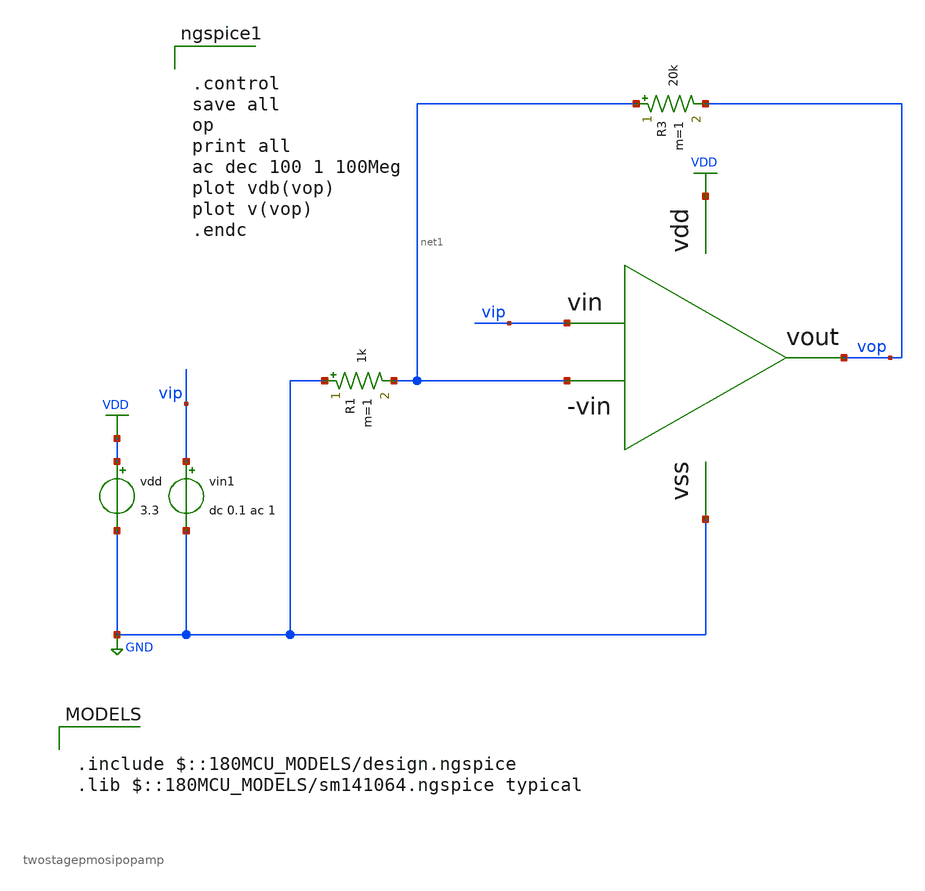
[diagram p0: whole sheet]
** sch_path: designs/libs/OTA/pmosota_VF_tb.sch
**.subckt pmosota_VF_tb
vdd VDD GND 3.3
xOTA1 vip VDD net1 vop GND twostagepmosipopamp
R3 net1 vop 20k m=1
R1 GND net1 1k m=1
vin1 vip GND dc 0.1 ac 1
**** begin user architecture code

.include $::180MCU_MODELS/design.ngspice
.lib $::180MCU_MODELS/sm141064.ngspice typical



.control
save all
op
print all
ac dec 100 1 100Meg
plot vdb(vop)
plot v(vop)
.endc

**** end user architecture code
**.ends
.GLOBAL GND
.GLOBAL VDD
.end
